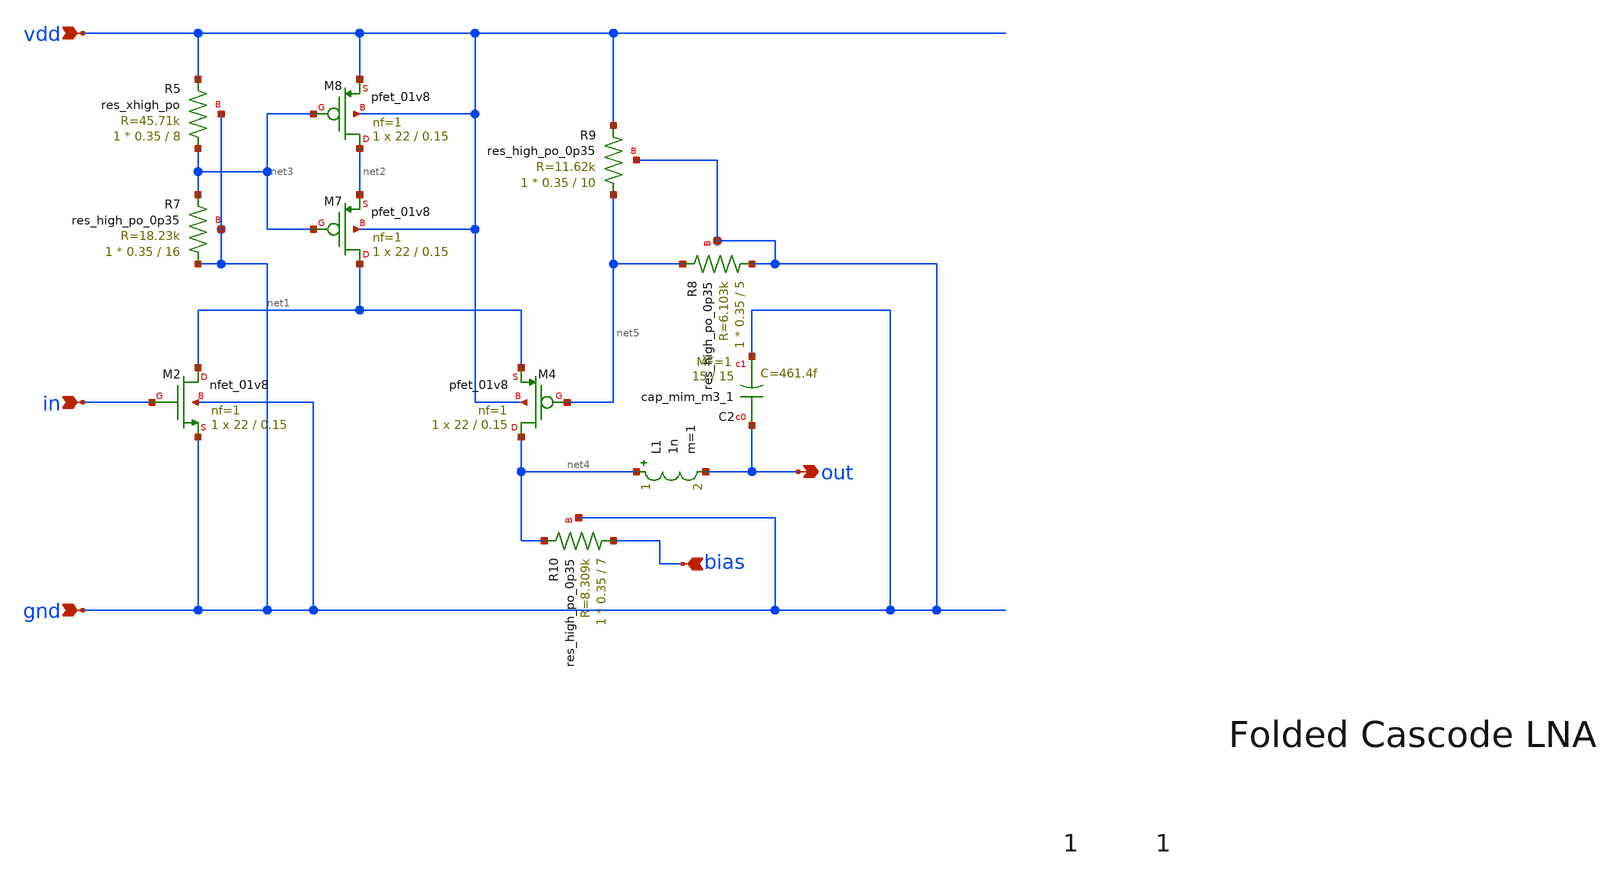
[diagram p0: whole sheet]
** sch_path: xschem/lna/foldedcascode.sch
**.subckt foldedcascode out vdd gnd in bias
*.opin out
*.ipin vdd
*.ipin gnd
*.ipin in
*.ipin bias
XM2 net1 in gnd gnd sky130_fd_pr__nfet_01v8 L=0.15 W=22 nf=1 ad='int((nf+1)/2) * W/nf * 0.29' as='int((nf+2)/2) * W/nf * 0.29'
+ pd='2*int((nf+1)/2) * (W/nf + 0.29)' ps='2*int((nf+2)/2) * (W/nf + 0.29)' nrd='0.29 / W' nrs='0.29 / W'
+ sa=0 sb=0 sd=0 mult=1 m=1
XM4 net4 net5 net1 vdd sky130_fd_pr__pfet_01v8 L=0.15 W=22 nf=1 ad='int((nf+1)/2) * W/nf * 0.29' as='int((nf+2)/2) * W/nf * 0.29'
+ pd='2*int((nf+1)/2) * (W/nf + 0.29)' ps='2*int((nf+2)/2) * (W/nf + 0.29)' nrd='0.29 / W' nrs='0.29 / W'
+ sa=0 sb=0 sd=0 mult=1 m=1
XM7 net1 net3 net2 vdd sky130_fd_pr__pfet_01v8 L=0.15 W=22 nf=1 ad='int((nf+1)/2) * W/nf * 0.29' as='int((nf+2)/2) * W/nf * 0.29'
+ pd='2*int((nf+1)/2) * (W/nf + 0.29)' ps='2*int((nf+2)/2) * (W/nf + 0.29)' nrd='0.29 / W' nrs='0.29 / W'
+ sa=0 sb=0 sd=0 mult=1 m=1
XM8 net2 net3 vdd vdd sky130_fd_pr__pfet_01v8 L=0.15 W=22 nf=1 ad='int((nf+1)/2) * W/nf * 0.29' as='int((nf+2)/2) * W/nf * 0.29'
+ pd='2*int((nf+1)/2) * (W/nf + 0.29)' ps='2*int((nf+2)/2) * (W/nf + 0.29)' nrd='0.29 / W' nrs='0.29 / W'
+ sa=0 sb=0 sd=0 mult=1 m=1
XC2 out gnd sky130_fd_pr__cap_mim_m3_1 W=15 L=15 MF=1 m=1
XR5 net3 vdd gnd sky130_fd_pr__res_xhigh_po W=0.35 L=8 mult=1 m=1
XR7 gnd net3 gnd sky130_fd_pr__res_high_po_0p35 L=16 mult=1 m=1
XR8 gnd net5 gnd sky130_fd_pr__res_high_po_0p35 L=5 mult=1 m=1
XR9 net5 vdd gnd sky130_fd_pr__res_high_po_0p35 L=10 mult=1 m=1
XR10 bias net4 gnd sky130_fd_pr__res_high_po_0p35 L=7 mult=1 m=1
L1 net4 out 1n m=1
**** begin user architecture code
 ** manual skywater pdks install (with patches applied)
* .lib $::SKYWATER_MODELS/models/sky130.lib.spice tt

** opencircuitdesign pdks install
.lib /foss/pdk/sky130A/libs.tech/ngspice/sky130.lib.spice tt

.param mc_mm_switch=0
.param mc_pr_switch=0

**** end user architecture code
**.ends
.end
